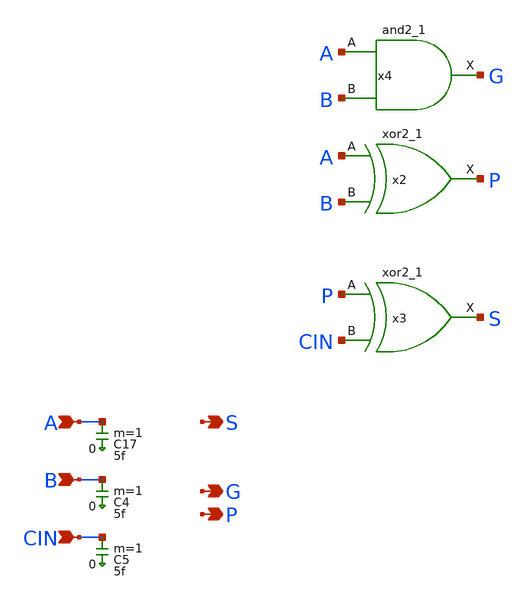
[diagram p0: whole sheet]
** sch_path: sky130A/xschem_libs/sky130_tests/adder_1bit/schematic/adder_1bit.sch
**.subckt adder_1bit A B CIN S P G
*.ipin A
*.ipin B
*.ipin CIN
*.opin S
*.opin P
*.opin G
x4 A B VSS VSS VCC VCC G sky130_fd_sc_hd__and2_1
x2 A B VSS VSS VCC VCC P sky130_fd_sc_hd__xor2_1
x3 P CIN VSS VSS VCC VCC S sky130_fd_sc_hd__xor2_1
C17 A 0 5f m=1
C4 B 0 5f m=1
C5 CIN 0 5f m=1
**.ends
.end
